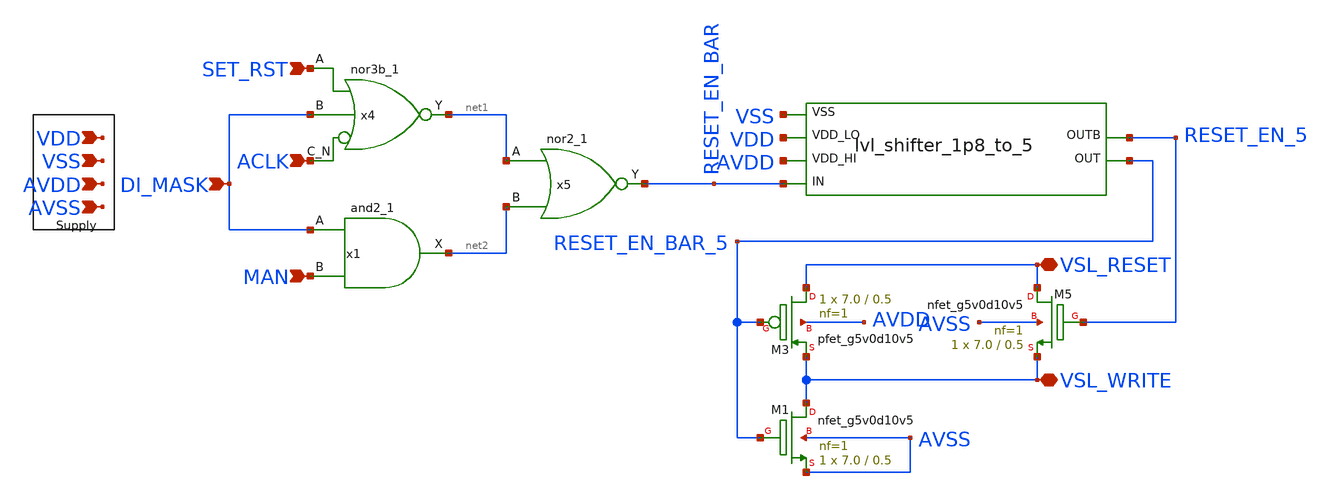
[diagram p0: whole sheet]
** sch_path: BL_SL_Writing_Interface/SL_driver.sch
**.subckt SL_driver VDD VSS MAN DI_MASK ACLK SET_RST AVDD AVSS VSL_RESET VSL_WRITE
*.ipin VDD
*.ipin VSS
*.ipin MAN
*.ipin DI_MASK
*.ipin ACLK
*.ipin SET_RST
*.ipin AVDD
*.ipin AVSS
*.iopin VSL_RESET
*.iopin VSL_WRITE
x4 SET_RST DI_MASK ACLK VSS VSS VDD VDD net1 sky130_fd_sc_hvl__nor3b_1
x5 net1 net2 VSS VSS VDD VDD RESET_EN_BAR sky130_fd_sc_hvl__nor2_1
x1 DI_MASK MAN VSS VSS VDD VDD net2 sky130_fd_sc_hd__and2_1
x1 AVDD RESET_EN_5 RESET_EN_BAR_5 VDD RESET_EN_BAR VSS lvl_shifter_1p8_to_5
XM3 VSL_RESET RESET_EN_BAR_5 VSL_WRITE AVDD sky130_fd_pr__pfet_g5v0d10v5 L=0.5 W=7.0 nf=1 ad='int((nf+1)/2) * W/nf * 0.29'
+ as='int((nf+2)/2) * W/nf * 0.29' pd='2*int((nf+1)/2) * (W/nf + 0.29)' ps='2*int((nf+2)/2) * (W/nf + 0.29)'
+ nrd='0.29 / W' nrs='0.29 / W' sa=0 sb=0 sd=0 mult=1 m=1
XM5 VSL_RESET RESET_EN_5 VSL_WRITE AVSS sky130_fd_pr__nfet_g5v0d10v5 L=0.5 W=7.0 nf=1 ad='int((nf+1)/2) * W/nf * 0.29'
+ as='int((nf+2)/2) * W/nf * 0.29' pd='2*int((nf+1)/2) * (W/nf + 0.29)' ps='2*int((nf+2)/2) * (W/nf + 0.29)'
+ nrd='0.29 / W' nrs='0.29 / W' sa=0 sb=0 sd=0 mult=1 m=1
XM1 VSL_WRITE RESET_EN_BAR_5 AVSS AVSS sky130_fd_pr__nfet_g5v0d10v5 L=0.5 W=7.0 nf=1 ad='int((nf+1)/2) * W/nf * 0.29'
+ as='int((nf+2)/2) * W/nf * 0.29' pd='2*int((nf+1)/2) * (W/nf + 0.29)' ps='2*int((nf+2)/2) * (W/nf + 0.29)'
+ nrd='0.29 / W' nrs='0.29 / W' sa=0 sb=0 sd=0 mult=1 m=1
**.ends

* expanding   symbol:  lvl_shifter_1p8_to_5.sym # of pins=6
** sym_path: BL_SL_Writing_Interface/lvl_shifter_1p8_to_5.sym
** sch_path: BL_SL_Writing_Interface/lvl_shifter_1p8_to_5.sch
.subckt lvl_shifter_1p8_to_5 VDD_HI OUTB OUT VDD_LO IN VSS
*.ipin VDD_HI
*.opin OUT
*.opin OUTB
*.ipin IN
*.ipin VDD_LO
*.ipin VSS
XM5 net1 IN VSS VSS sky130_fd_pr__nfet_01v8 L=0.15 W=0.42 nf=1 ad='int((nf+1)/2) * W/nf * 0.29' as='int((nf+2)/2) * W/nf * 0.29'
+ pd='2*int((nf+1)/2) * (W/nf + 0.29)' ps='2*int((nf+2)/2) * (W/nf + 0.29)' nrd='0.29 / W' nrs='0.29 / W'
+ sa=0 sb=0 sd=0 mult=1 m=1
XM7 net2 net1 VSS VSS sky130_fd_pr__nfet_01v8 L=0.15 W=0.42 nf=1 ad='int((nf+1)/2) * W/nf * 0.29' as='int((nf+2)/2) * W/nf * 0.29'
+ pd='2*int((nf+1)/2) * (W/nf + 0.29)' ps='2*int((nf+2)/2) * (W/nf + 0.29)' nrd='0.29 / W' nrs='0.29 / W'
+ sa=0 sb=0 sd=0 mult=1 m=1
XM3 net1 IN VDD_LO VDD_LO sky130_fd_pr__pfet_01v8 L=0.15 W=0.84 nf=1 ad='int((nf+1)/2) * W/nf * 0.29'
+ as='int((nf+2)/2) * W/nf * 0.29' pd='2*int((nf+1)/2) * (W/nf + 0.29)' ps='2*int((nf+2)/2) * (W/nf + 0.29)'
+ nrd='0.29 / W' nrs='0.29 / W' sa=0 sb=0 sd=0 mult=1 m=1
XM4 net2 net1 VDD_LO VDD_LO sky130_fd_pr__pfet_01v8 L=0.15 W=0.84 nf=1 ad='int((nf+1)/2) * W/nf * 0.29'
+ as='int((nf+2)/2) * W/nf * 0.29' pd='2*int((nf+1)/2) * (W/nf + 0.29)' ps='2*int((nf+2)/2) * (W/nf + 0.29)'
+ nrd='0.29 / W' nrs='0.29 / W' sa=0 sb=0 sd=0 mult=1 m=1
XM6 OUT net1 VSS VSS sky130_fd_pr__nfet_g5v0d10v5 L=0.5 W=5 nf=1 ad='int((nf+1)/2) * W/nf * 0.29' as='int((nf+2)/2) * W/nf * 0.29'
+ pd='2*int((nf+1)/2) * (W/nf + 0.29)' ps='2*int((nf+2)/2) * (W/nf + 0.29)' nrd='0.29 / W' nrs='0.29 / W'
+ sa=0 sb=0 sd=0 mult=1 m=1
XM8 OUTB net2 VSS VSS sky130_fd_pr__nfet_g5v0d10v5 L=0.5 W=5 nf=1 ad='int((nf+1)/2) * W/nf * 0.29' as='int((nf+2)/2) * W/nf * 0.29'
+ pd='2*int((nf+1)/2) * (W/nf + 0.29)' ps='2*int((nf+2)/2) * (W/nf + 0.29)' nrd='0.29 / W' nrs='0.29 / W'
+ sa=0 sb=0 sd=0 mult=1 m=1
XM1 OUT OUTB VDD_HI VDD_HI sky130_fd_pr__pfet_g5v0d10v5 L=0.5 W=1.5 nf=1 ad='int((nf+1)/2) * W/nf * 0.29'
+ as='int((nf+2)/2) * W/nf * 0.29' pd='2*int((nf+1)/2) * (W/nf + 0.29)' ps='2*int((nf+2)/2) * (W/nf + 0.29)'
+ nrd='0.29 / W' nrs='0.29 / W' sa=0 sb=0 sd=0 mult=1 m=1
XM2 OUTB OUT VDD_HI VDD_HI sky130_fd_pr__pfet_g5v0d10v5 L=0.5 W=1.5 nf=1 ad='int((nf+1)/2) * W/nf * 0.29'
+ as='int((nf+2)/2) * W/nf * 0.29' pd='2*int((nf+1)/2) * (W/nf + 0.29)' ps='2*int((nf+2)/2) * (W/nf + 0.29)'
+ nrd='0.29 / W' nrs='0.29 / W' sa=0 sb=0 sd=0 mult=1 m=1
.ends

.end
